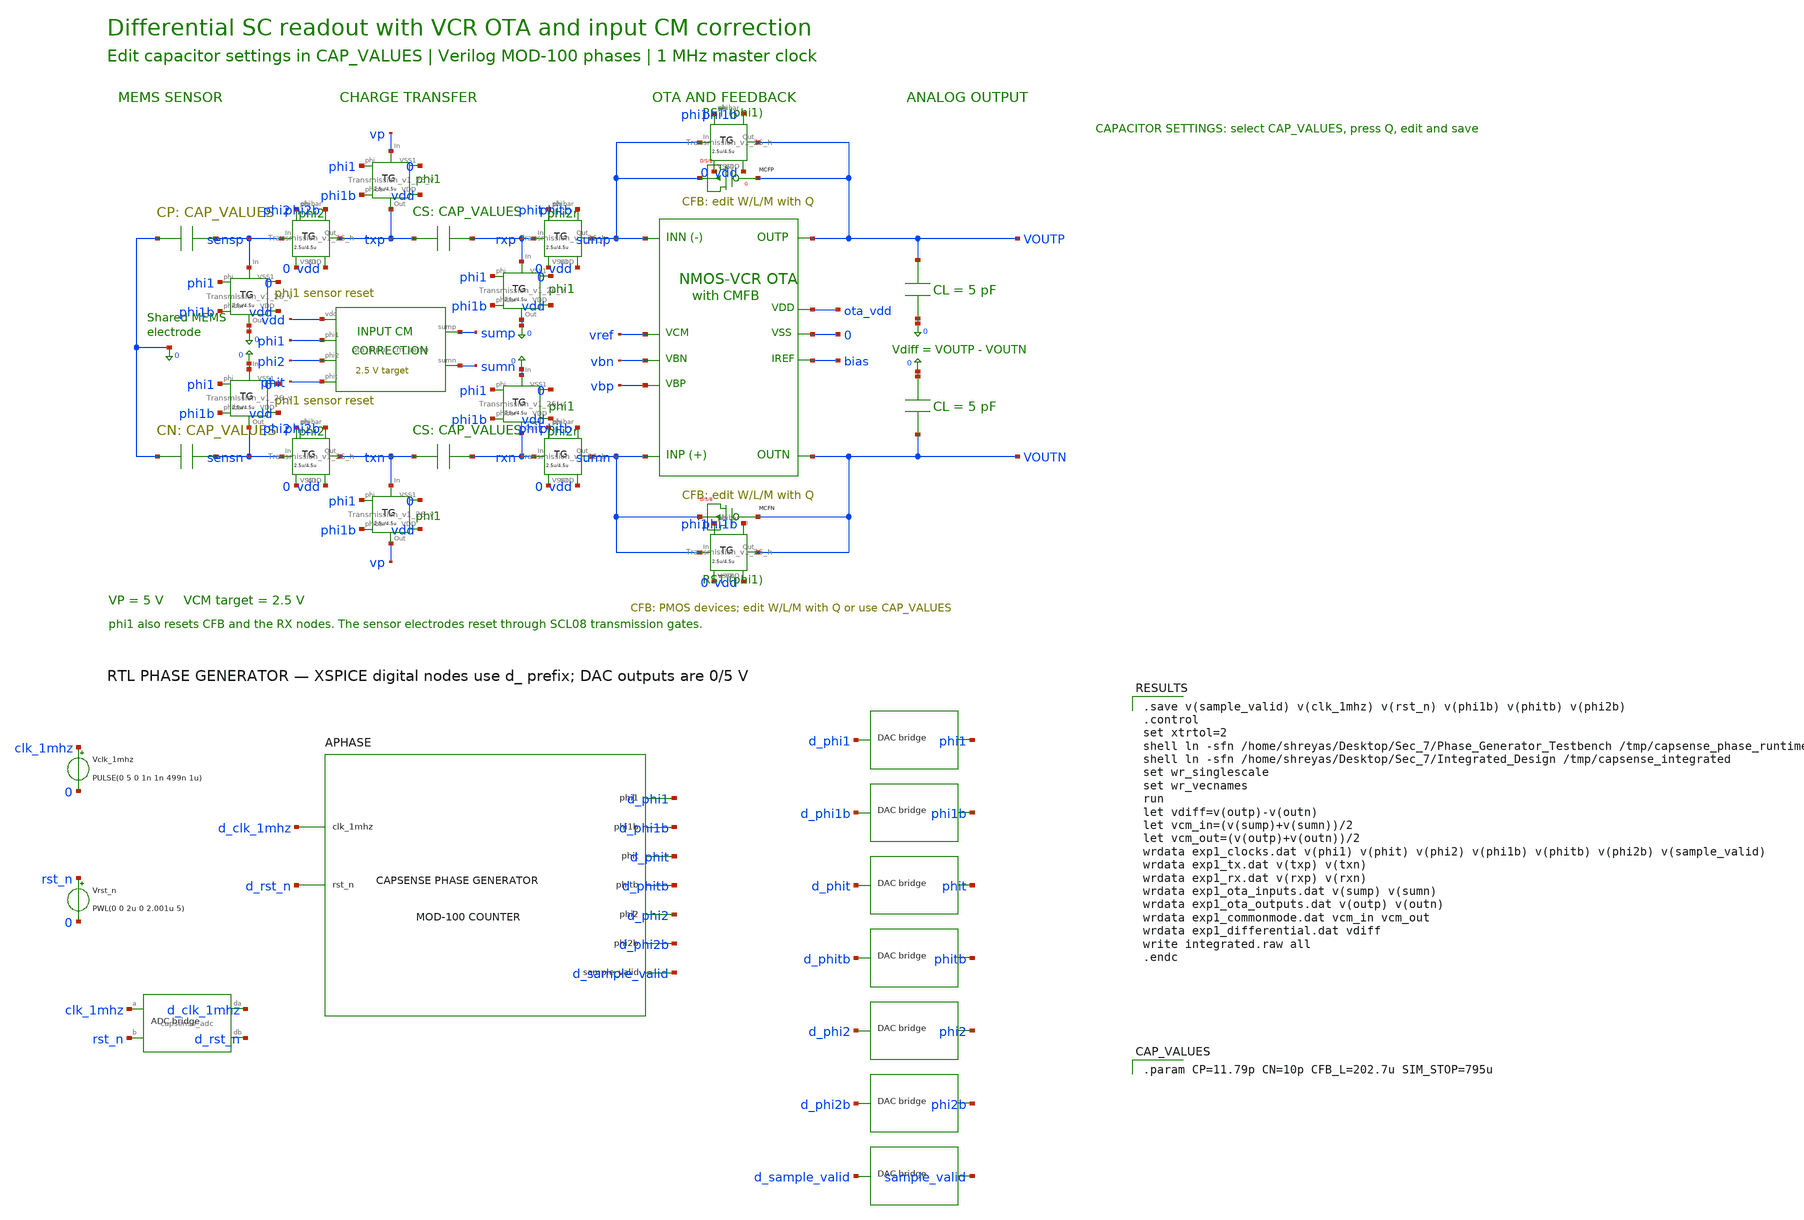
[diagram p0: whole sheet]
** sch_path: Mixed_Signal/Integrated_Design/schematic/capsense_integrated_tb.sch
**.subckt capsense_integrated_tb
XOTA sumn sump outp outn ota_vdd 0 bias vref vbn vbp ota_telescopic_cm2p5
CMEMP 0 sensp {CP}
XSENSEP phi2 0 sensp txp vdd phi2b Transmission_v1_26_h
XSRESETP phi1 0 sensp 0 vdd phi1b Transmission_v1_26_v
XCHARGEP phi1 0 vp txp vdd phi1b Transmission_v1_26_v
CSP txp rxp {CS}
XRRESETP phi1 0 rxp 0 vdd phi1b Transmission_v1_26_v
XXFERP phit 0 rxp sump vdd phitb Transmission_v1_26_h
MCFP sump outp sump sump P W={CFB_W} L={CFB_L} M={CFB_M} AD='( {CFB_W} ) * 4.5u' AS='( {CFB_W} ) * 4.5u'
+ PD='2 * ( {CFB_W} ) + 9u' PS='2 * ( {CFB_W} ) + 9u'
XFBRESETP phi1 0 sump outp vdd phi1b Transmission_v1_26_h
CLP outp 0 5p
CMEMN 0 sensn {CN}
XSENSEN phi2 0 sensn txn vdd phi2b Transmission_v1_26_h
XSRESETN phi1 0 0 sensn vdd phi1b Transmission_v1_26_v
XCHARGEN phi1 0 txn vp vdd phi1b Transmission_v1_26_v
CSN txn rxn {CS}
XRRESETN phi1 0 0 rxn vdd phi1b Transmission_v1_26_v
XXFERN phit 0 rxn sumn vdd phitb Transmission_v1_26_h
MCFN sumn outn sumn sumn P W={CFB_W} L={CFB_L} M={CFB_M} AD='( {CFB_W} ) * 4.5u' AS='( {CFB_W} ) * 4.5u'
+ PD='2 * ( {CFB_W} ) + 9u' PS='2 * ( {CFB_W} ) + 9u'
XFBRESETN phi1 0 sumn outn vdd phi1b Transmission_v1_26_h
CLN 0 outn 5p
XICM sump sumn vdd phi1 phi2 phit ota_input_cm_servo
APHASE [ d_clk_1mhz d_rst_n ] [ d_phi1 d_phit d_phi2 d_phi1b d_phitb d_phi2b d_sample_valid ] null
+ capsense_phase_gen_cosim
Vclk_1mhz clk_1mhz 0 PULSE(0 5 0 1n 1n 499n 1u)
Vrst_n rst_n 0 PWL(0 0 2u 0 2.001u 5)
AINPUTS [ clk_1mhz rst_n ] [ d_clk_1mhz d_rst_n ] capsense_adc
ADAC_phi1 [ d_phi1 ] [ phi1 ] capsense_dac
ADAC_phi1b [ d_phi1b ] [ phi1b ] capsense_dac
ADAC_phit [ d_phit ] [ phit ] capsense_dac
ADAC_phitb [ d_phitb ] [ phitb ] capsense_dac
ADAC_phi2 [ d_phi2 ] [ phi2 ] capsense_dac
ADAC_phi2b [ d_phi2b ] [ phi2b ] capsense_dac
ADAC_sample_valid [ d_sample_valid ] [ sample_valid ] capsense_dac
**** begin user architecture code
.include /home/shreyas/Desktop/Sec_7/Integrated_Design/simulation/analog_support.spice
.include /home/shreyas/Desktop/Sec_7/Integrated_Design/simulation/cosim_models.spice

.save v(sample_valid) v(clk_1mhz) v(rst_n) v(phi1b) v(phitb) v(phi2b)
.control
set xtrtol=2
shell ln -sfn /home/shreyas/Desktop/Sec_7/Phase_Generator_Testbench /tmp/capsense_phase_runtime
shell ln -sfn /home/shreyas/Desktop/Sec_7/Integrated_Design /tmp/capsense_integrated
set wr_singlescale
set wr_vecnames
run
let vdiff=v(outp)-v(outn)
let vcm_in=(v(sump)+v(sumn))/2
let vcm_out=(v(outp)+v(outn))/2
wrdata exp1_clocks.dat v(phi1) v(phit) v(phi2) v(phi1b) v(phitb) v(phi2b) v(sample_valid)
wrdata exp1_tx.dat v(txp) v(txn)
wrdata exp1_rx.dat v(rxp) v(rxn)
wrdata exp1_ota_inputs.dat v(sump) v(sumn)
wrdata exp1_ota_outputs.dat v(outp) v(outn)
wrdata exp1_commonmode.dat vcm_in vcm_out
wrdata exp1_differential.dat vdiff
write integrated.raw all
.endc


.param CP=11.79p CN=10p CFB_L=202.7u SIM_STOP=795u

**** end user architecture code
**.ends
.end
